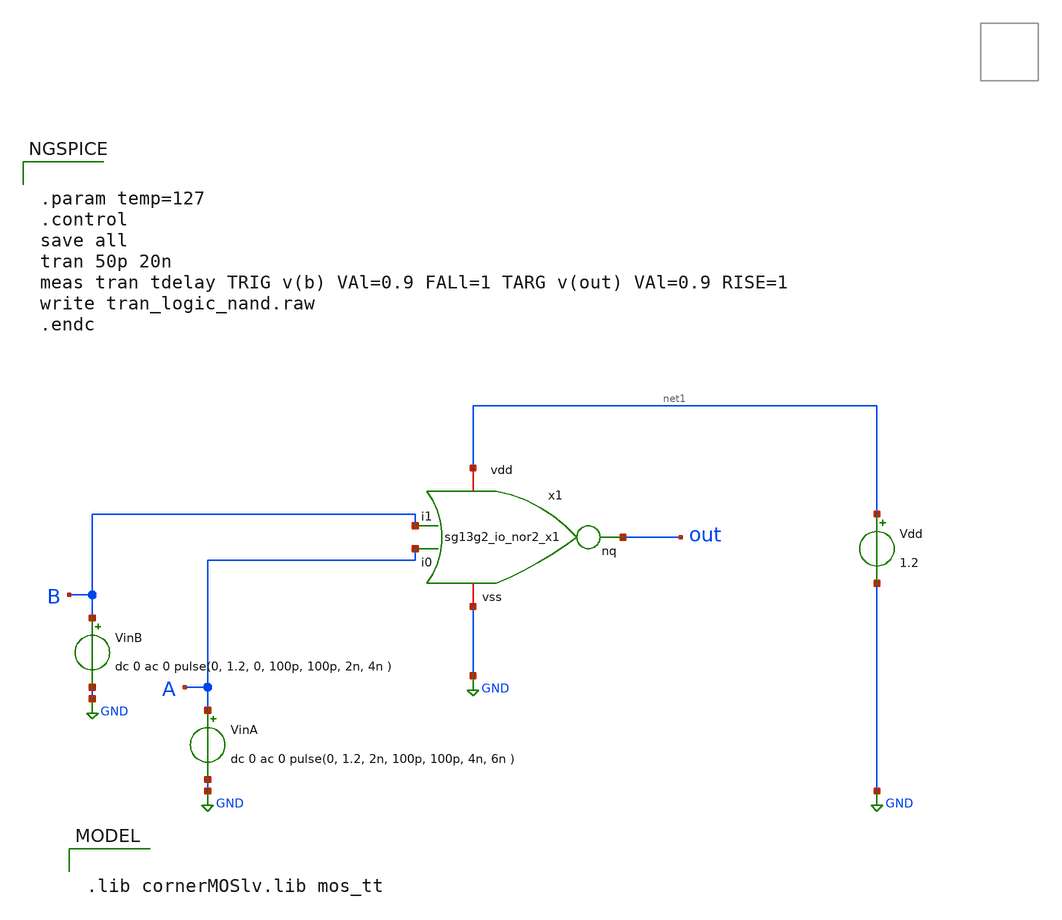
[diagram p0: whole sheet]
** sch_path: ihp-sg13g2/libs.ref/sg13g2_io/xschem/io_testbench/sg13g2_io_nor2_x1_tb.sch
* Copyright 2023 IHP PDK Authors
**.subckt sg13g2_io_nor2_x1_tb
VinA A GND dc 0 ac 0 pulse(0, 1.2, 2n, 100p, 100p, 4n, 6n )
Vdd net1 GND 1.2
VinB B GND dc 0 ac 0 pulse(0, 1.2, 0, 100p, 100p, 2n, 4n )
x1 net1 A out B GND sg13g2_io_nor2_x1
**** begin user architecture code

.lib cornerMOSlv.lib mos_tt



.param temp=127
.control
save all
tran 50p 20n
meas tran tdelay TRIG v(b) VAl=0.9 FALl=1 TARG v(out) VAl=0.9 RISE=1
write tran_logic_nand.raw
.endc


**** end user architecture code
**.ends
.GLOBAL GND
.end
